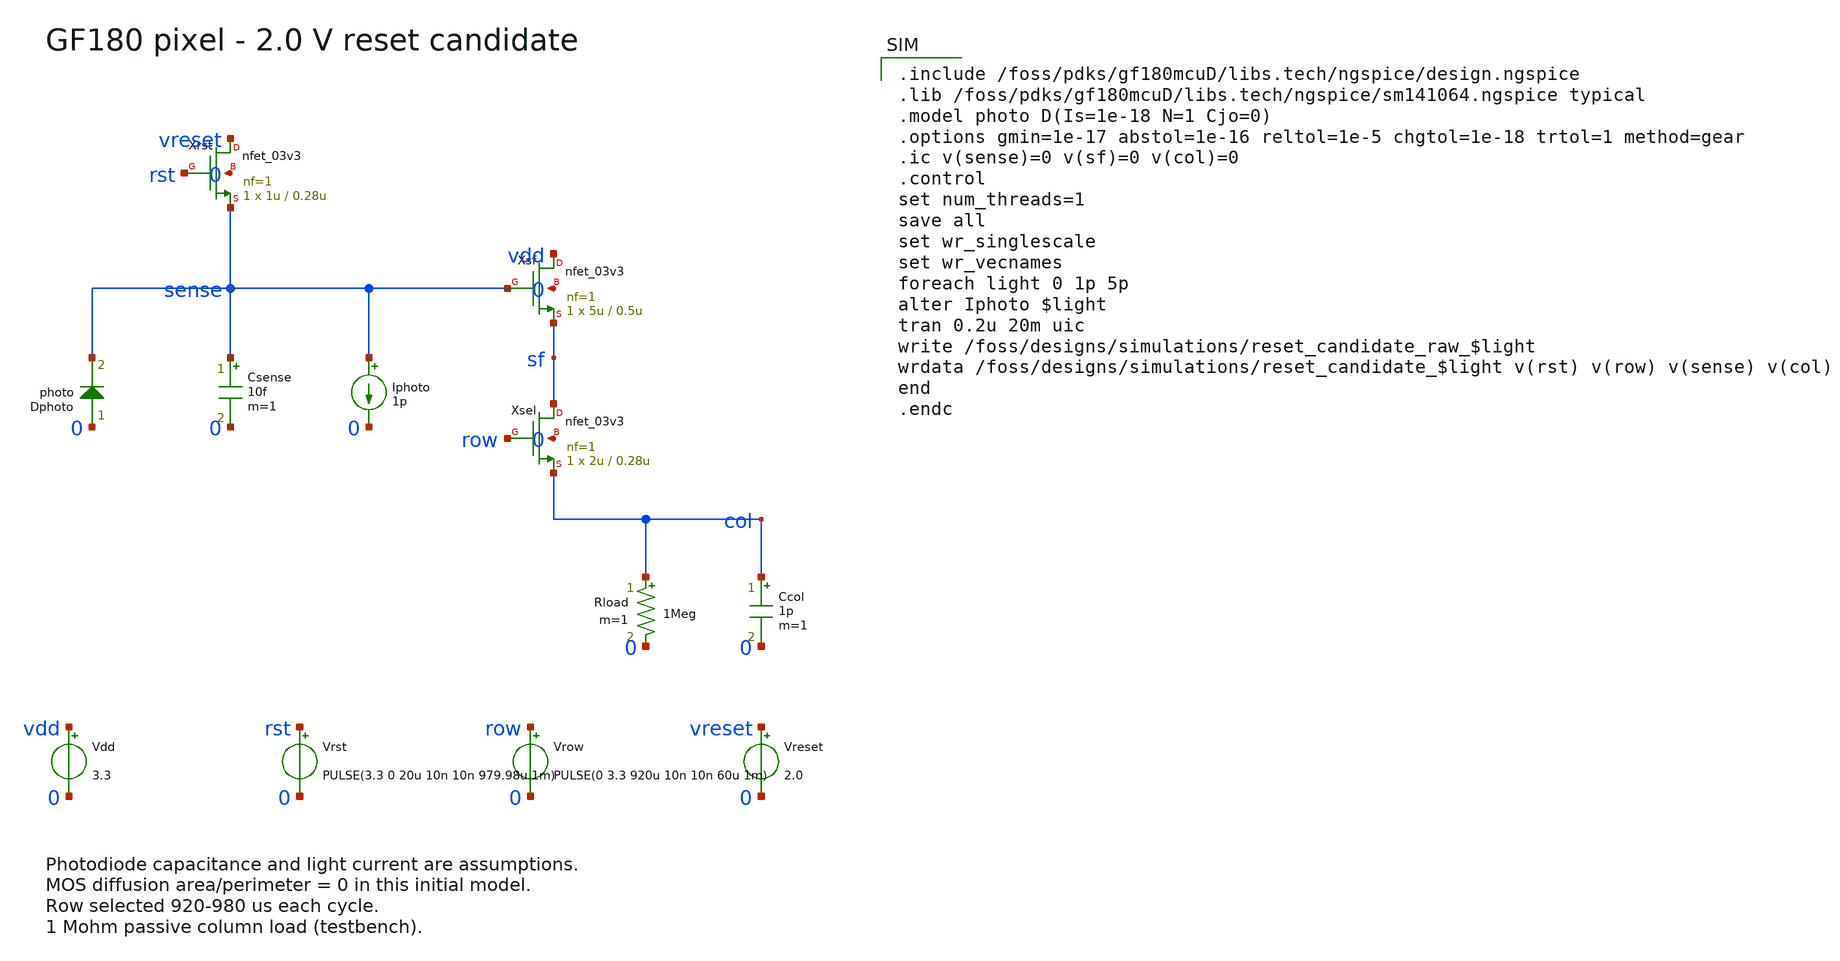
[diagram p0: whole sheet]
** sch_path: xschem/pixel_reset_candidate.sch
**.subckt pixel_reset_candidate
Xrst vreset rst sense 0 nfet_03v3 L=0.28u W=1u nf=1 ad=0 as=0 pd=0 ps=0 nrd=0 nrs=0 sa=0 sb=0 sd=0
+ m=1
Xsf vdd sense sf 0 nfet_03v3 L=0.5u W=5u nf=1 ad=0 as=0 pd=0 ps=0 nrd=0 nrs=0 sa=0 sb=0 sd=0 m=1
Xsel sf row col 0 nfet_03v3 L=0.28u W=2u nf=1 ad=0 as=0 pd=0 ps=0 nrd=0 nrs=0 sa=0 sb=0 sd=0 m=1
Dphoto 0 sense photo area=1
Csense sense 0 10f m=1
Iphoto sense 0 1p
Rload col 0 1Meg m=1
Ccol col 0 1p m=1
Vdd vdd 0 3.3
Vrst rst 0 PULSE(3.3 0 20u 10n 10n 979.98u 1m)
Vrow row 0 PULSE(0 3.3 920u 10n 10n 60u 1m)
Vreset vreset 0 2.0
**** begin user architecture code

.include /foss/pdks/gf180mcuD/libs.tech/ngspice/design.ngspice
.lib /foss/pdks/gf180mcuD/libs.tech/ngspice/sm141064.ngspice typical
.model photo D(Is=1e-18 N=1 Cjo=0)
.options gmin=1e-17 abstol=1e-16 reltol=1e-5 chgtol=1e-18 trtol=1 method=gear
.ic v(sense)=0 v(sf)=0 v(col)=0
.control
set num_threads=1
save all
set wr_singlescale
set wr_vecnames
foreach light 0 1p 5p
alter Iphoto $light
tran 0.2u 20m uic
write /foss/designs/simulations/reset_candidate_raw_$light
wrdata /foss/designs/simulations/reset_candidate_$light v(rst) v(row) v(sense) v(col)
end
.endc

**** end user architecture code
**.ends
.end
